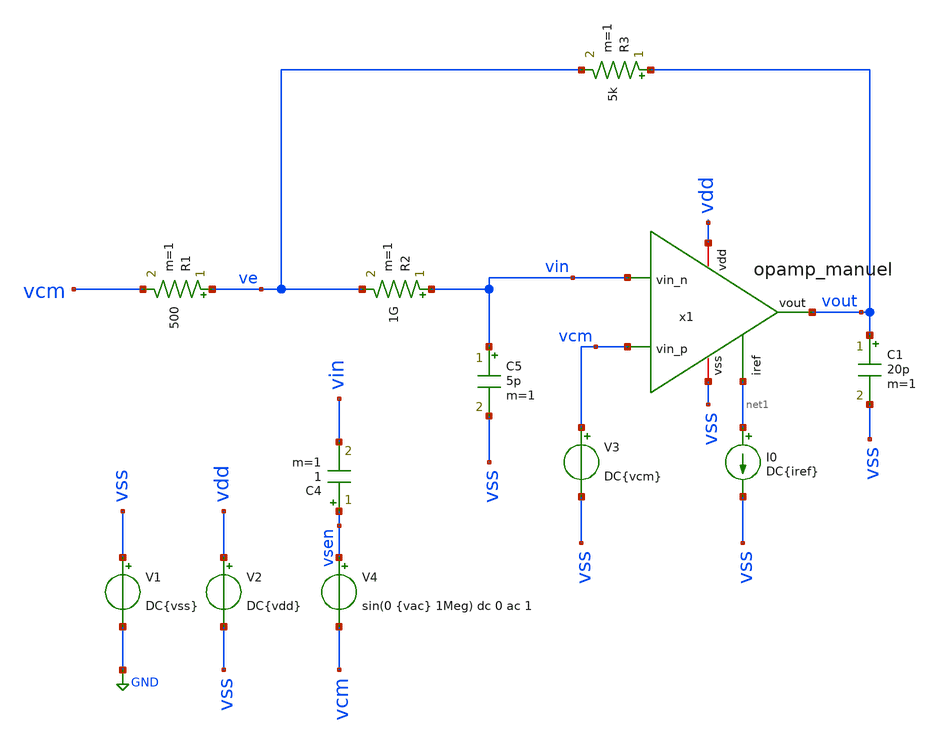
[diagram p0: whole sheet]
** sch_path: track_analogico/opamp_manuel/sch/opamp_openloop.sch
**.subckt opamp_openloop
V1 vss GND DC{vss}
V2 vdd vss DC{vdd}
V3 vcm vss DC{vcm}
V4 vsen vcm sin(0 {vac} 1Meg) dc 0 ac 1
C4 vsen vin 1 m=1
I0 net1 vss DC{iref}
R1 ve vcm 500 m=1
R2 vin ve 1G m=1
R3 vout ve 5k m=1
C5 vin vss 5p m=1
C1 vout vss 20p m=1
x1 vdd net1 vin vcm vout vss opamp_manuel
**** begin user architecture code




* Circuit Parameters
.param vss = 0
.param vdd = 1.8
.param vac = 0.2
.param vcm = vdd/2
.param iref = 100u

.options TEMP = 65

* Include Models
.lib ~/skywater/skywater-pdk/libraries/sky130_fd_pr_ngspice/latest/models/corners/sky130.lib TT

* OP Parameters & Signals to save
.save all  @M.X1.XM1.msky130_fd_pr__pfet_01v8_lvt[id] @M.X1.XM1.msky130_fd_pr__pfet_01v8_lvt[vth] @M.X1.XM1.msky130_fd_pr__pfet_01v8_lvt[vgs] @M.X1.XM1.msky130_fd_pr__pfet_01v8_lvt[vds] @M.X1.XM1.msky130_fd_pr__pfet_01v8_lvt[vdsat] @M.X1.XM1.msky130_fd_pr__pfet_01v8_lvt[gm] @M.X1.XM1.msky130_fd_pr__pfet_01v8_lvt[gds]  @M.X1.XM2.msky130_fd_pr__pfet_01v8_lvt[id] @M.X1.XM2.msky130_fd_pr__pfet_01v8_lvt[vth] @M.X1.XM2.msky130_fd_pr__pfet_01v8_lvt[vgs] @M.X1.XM2.msky130_fd_pr__pfet_01v8_lvt[vds] @M.X1.XM2.msky130_fd_pr__pfet_01v8_lvt[vdsat] @M.X1.XM2.msky130_fd_pr__pfet_01v8_lvt[gm] @M.X1.XM2.msky130_fd_pr__pfet_01v8_lvt[gds]  @M.X1.XM3.msky130_fd_pr__nfet_01v8[id] @M.X1.XM3.msky130_fd_pr__nfet_01v8[vth] @M.X1.XM3.msky130_fd_pr__nfet_01v8[vgs] @M.X1.XM3.msky130_fd_pr__nfet_01v8[vds] @M.X1.XM3.msky130_fd_pr__nfet_01v8[vdsat] @M.X1.XM3.msky130_fd_pr__nfet_01v8[gm] @M.X1.XM3.msky130_fd_pr__nfet_01v8[gds]  @M.X1.XM4.msky130_fd_pr__nfet_01v8[id] @M.X1.XM4.msky130_fd_pr__nfet_01v8[vth] @M.X1.XM4.msky130_fd_pr__nfet_01v8[vgs] @M.X1.XM4.msky130_fd_pr__nfet_01v8[vds] @M.X1.XM4.msky130_fd_pr__nfet_01v8[vdsat] @M.X1.XM4.msky130_fd_pr__nfet_01v8[gm] @M.X1.XM4.msky130_fd_pr__nfet_01v8[gds]  @M.X1.XM5.msky130_fd_pr__pfet_01v8[id] @M.X1.XM5.msky130_fd_pr__pfet_01v8[vth] @M.X1.XM5.msky130_fd_pr__pfet_01v8[vgs] @M.X1.XM5.msky130_fd_pr__pfet_01v8[vds] @M.X1.XM5.msky130_fd_pr__pfet_01v8[vdsat] @M.X1.XM5.msky130_fd_pr__pfet_01v8[gm] @M.X1.XM5.msky130_fd_pr__pfet_01v8[gds]  @M.X1.XM6.msky130_fd_pr__nfet_01v8[id] @M.X1.XM6.msky130_fd_pr__nfet_01v8[vth] @M.X1.XM6.msky130_fd_pr__nfet_01v8[vgs] @M.X1.XM6.msky130_fd_pr__nfet_01v8[vds] @M.X1.XM6.msky130_fd_pr__nfet_01v8[vdsat] @M.X1.XM6.msky130_fd_pr__nfet_01v8[gm] @M.X1.XM6.msky130_fd_pr__nfet_01v8[gds]  @M.X1.XM7.msky130_fd_pr__pfet_01v8[id] @M.X1.XM7.msky130_fd_pr__pfet_01v8[vth] @M.X1.XM7.msky130_fd_pr__pfet_01v8[vgs] @M.X1.XM7.msky130_fd_pr__pfet_01v8[vds] @M.X1.XM7.msky130_fd_pr__pfet_01v8[vdsat] @M.X1.XM7.msky130_fd_pr__pfet_01v8[gm] @M.X1.XM7.msky130_fd_pr__pfet_01v8[gds]  @M.X1.XM8.msky130_fd_pr__pfet_01v8[id] @M.X1.XM8.msky130_fd_pr__pfet_01v8[vth] @M.X1.XM8.msky130_fd_pr__pfet_01v8[vgs] @M.X1.XM8.msky130_fd_pr__pfet_01v8[vds] @M.X1.XM8.msky130_fd_pr__pfet_01v8[vdsat] @M.X1.XM8.msky130_fd_pr__pfet_01v8[gm] @M.X1.XM8.msky130_fd_pr__pfet_01v8[gds]  @M.X1.XM6.msky130_fd_pr__nfet_01v8[cgs]  @M.X1.XM9.msky130_fd_pr__nfet_01v8[gds]

*Simulation
.control

* analisis AC
	ac dec 100 1k 500G

 	meas ac DCG find vdb(vout) at=2k
	meas ac GBW when vdb(vout)=0
	meas ac PM find vp(vout) when vdb(vout)=0

	print GBW
	print DCG
	print PM*180/PI

	plot vdb(vout) vp(vout)*180/PI title 'Transferencia a lazo abierto'

	write opamp_openloop.raw

* analisis de operación
	reset
	op
	save all

	print @M.X1.XM9.msky130_fd_pr__nfet_01v8[gds]
	write opamp_openloop.raw
.endc

.end


**** end user architecture code
**.ends
.GLOBAL GND
.end
